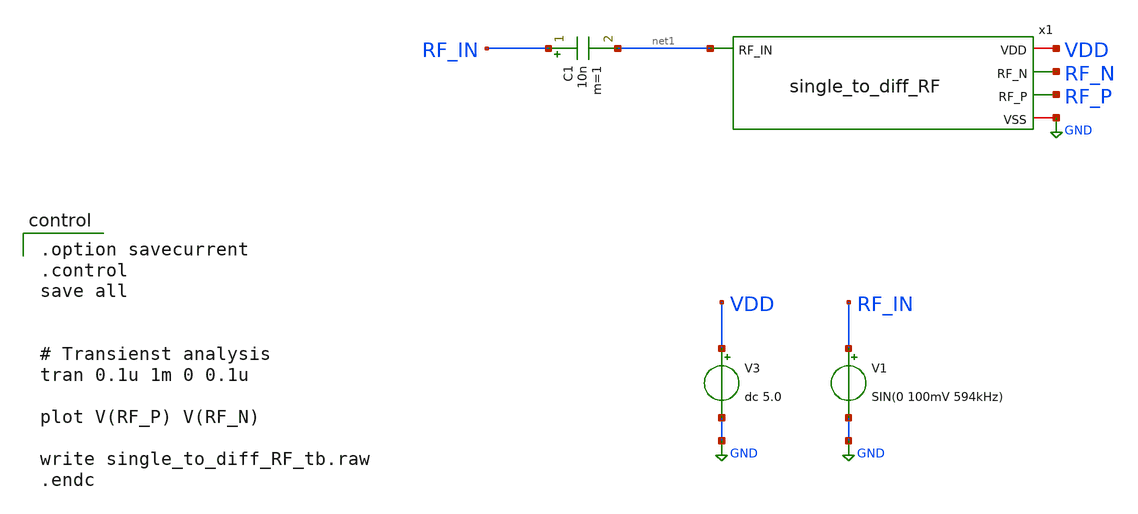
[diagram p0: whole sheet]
** sch_path: member_project/MIXER/noritsuna/xschem/single_to_diff_RF_tb.sch
**.subckt single_to_diff_RF_tb
x1 VDD RF_N net1 RF_P GND single_to_diff_RF
V3 VDD GND dc 5.0
C1 RF_IN net1 10n m=1
V1 RF_IN GND SIN(0 100mV 594kHz)
**** begin user architecture code
 .include $::LIB/ip62_models

.option savecurrent
.control
save all


# Transienst analysis
tran 0.1u 1m 0 0.1u

plot V(RF_P) V(RF_N)

write single_to_diff_RF_tb.raw
.endc

**** end user architecture code
**.ends

* expanding   symbol:  single_to_diff_RF.sym # of pins=5
** sym_path: member_project/MIXER/noritsuna/xschem/single_to_diff_RF.sym
** sch_path: member_project/MIXER/noritsuna/xschem/single_to_diff_RF.sch
.subckt single_to_diff_RF VDD RF_N RF_IN RF_P VSS
*.iopin VDD
*.iopin VSS
*.opin RF_N
*.opin RF_P
*.ipin RF_IN
XXM1 RF_N RF_IN RF_P VSS NMOS w=50u l=2u nrd=0 nrs=0 m=1
XR1 VDD RF_N VDD F_RR w=2.8e-06 l=17.8e-06 R=5e+03 tc1=0 tc2=0 m=1
XR2 RF_P VSS VDD F_RR w=2.8e-06 l=17.8e-06 R=5e+03 tc1=0 tc2=0 m=1
XR3 VDD RF_IN VDD F_RR w=2.8e-06 l=49.2e-06 R=20e+03 tc1=0 tc2=0 m=1
XR4 net1 VSS VDD F_RR w=2.8e-06 l=49.2e-06 R=40e+03 tc1=0 tc2=0 m=1
XXM6 RF_N VSS VSS VSS NMOS w=5u l=2u nrd=0 nrs=0 m=2
XR5 RF_IN net1 VDD F_RR w=2.8e-06 l=49.2e-06 R=40e+03 tc1=0 tc2=0 m=1
.ends

.GLOBAL GND
.end
